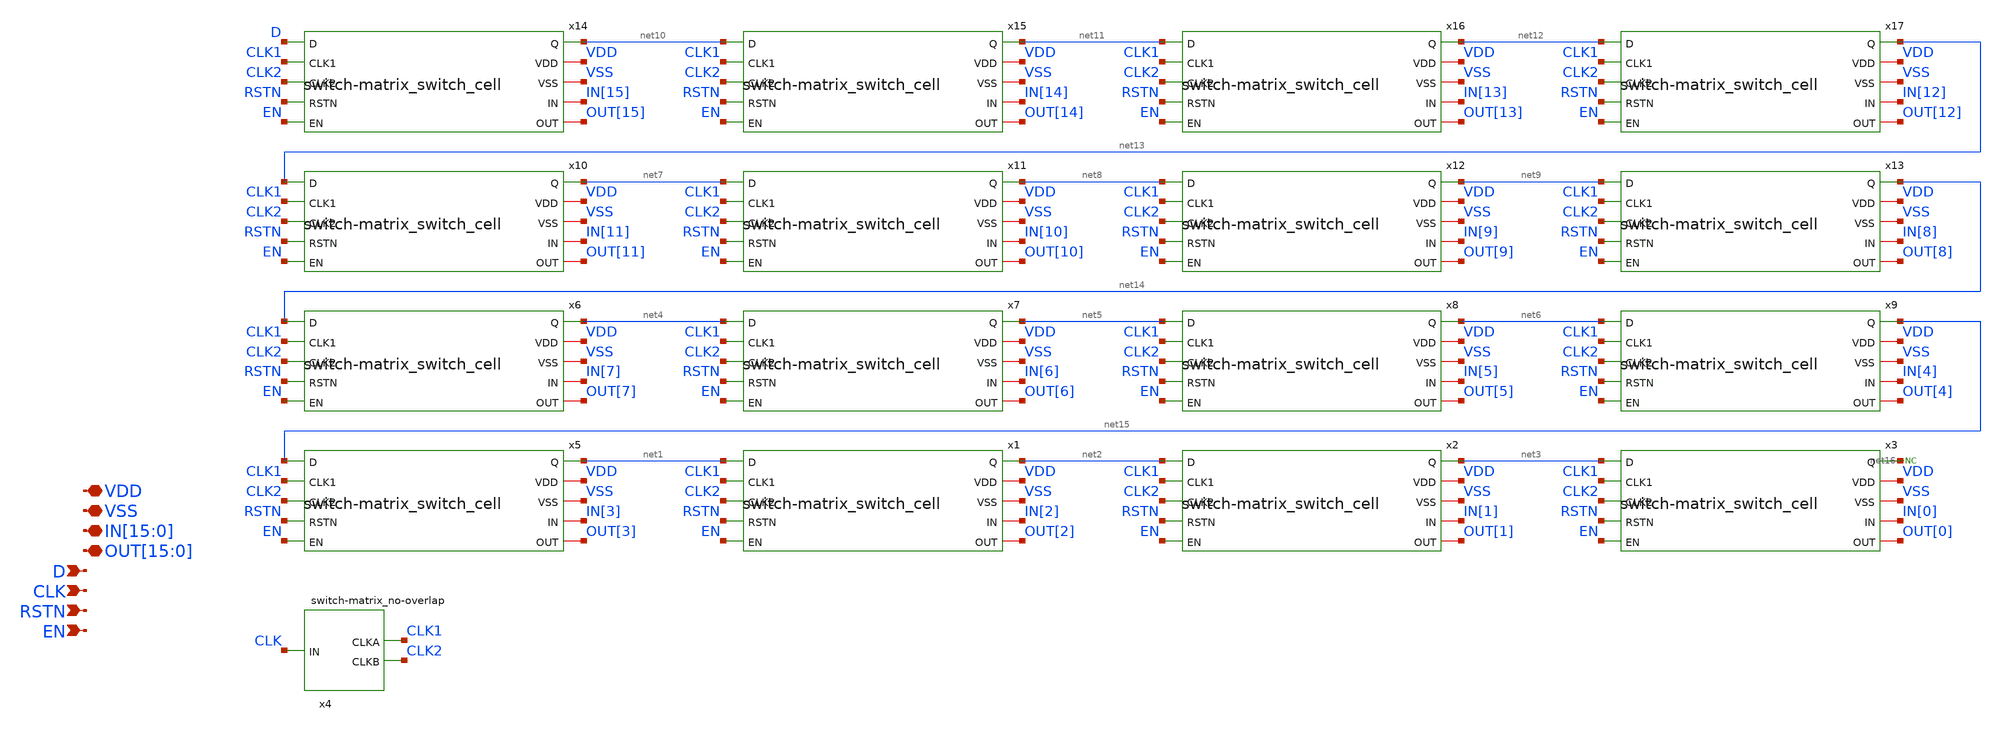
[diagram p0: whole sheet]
** sch_path: designs/libs/core_analog/switch-matrix/switch-matrix_tg_array_16x1.sch
**.subckt switch-matrix_tg_array_16x1 VDD VSS
*+ IN[15],IN[14],IN[13],IN[12],IN[11],IN[10],IN[9],IN[8],IN[7],IN[6],IN[5],IN[4],IN[3],IN[2],IN[1],IN[0]
*+ OUT[15],OUT[14],OUT[13],OUT[12],OUT[11],OUT[10],OUT[9],OUT[8],OUT[7],OUT[6],OUT[5],OUT[4],OUT[3],OUT[2],OUT[1],OUT[0] D RSTN CLK EN
*.iopin VDD
*.iopin VSS
*.iopin
*+ IN[15],IN[14],IN[13],IN[12],IN[11],IN[10],IN[9],IN[8],IN[7],IN[6],IN[5],IN[4],IN[3],IN[2],IN[1],IN[0]
*.iopin
*+ OUT[15],OUT[14],OUT[13],OUT[12],OUT[11],OUT[10],OUT[9],OUT[8],OUT[7],OUT[6],OUT[5],OUT[4],OUT[3],OUT[2],OUT[1],OUT[0]
*.ipin D
*.ipin RSTN
*.ipin CLK
*.ipin EN
* noconn #net16
x5 net1 VDD VSS net15 CLK1 CLK2 RSTN EN IN[3] OUT[3] switch-matrix_switch_cell
x1 net2 VDD VSS net1 CLK1 CLK2 RSTN EN IN[2] OUT[2] switch-matrix_switch_cell
x2 net3 VDD VSS net2 CLK1 CLK2 RSTN EN IN[1] OUT[1] switch-matrix_switch_cell
x3 net16 VDD VSS net3 CLK1 CLK2 RSTN EN IN[0] OUT[0] switch-matrix_switch_cell
x4 CLK VSS VDD CLK1 CLK2 switch-matrix_no-overlap
x6 net4 VDD VSS net14 CLK1 CLK2 RSTN EN IN[7] OUT[7] switch-matrix_switch_cell
x7 net5 VDD VSS net4 CLK1 CLK2 RSTN EN IN[6] OUT[6] switch-matrix_switch_cell
x8 net6 VDD VSS net5 CLK1 CLK2 RSTN EN IN[5] OUT[5] switch-matrix_switch_cell
x9 net15 VDD VSS net6 CLK1 CLK2 RSTN EN IN[4] OUT[4] switch-matrix_switch_cell
x10 net7 VDD VSS net13 CLK1 CLK2 RSTN EN IN[11] OUT[11] switch-matrix_switch_cell
x11 net8 VDD VSS net7 CLK1 CLK2 RSTN EN IN[10] OUT[10] switch-matrix_switch_cell
x12 net9 VDD VSS net8 CLK1 CLK2 RSTN EN IN[9] OUT[9] switch-matrix_switch_cell
x13 net14 VDD VSS net9 CLK1 CLK2 RSTN EN IN[8] OUT[8] switch-matrix_switch_cell
x14 net10 VDD VSS D CLK1 CLK2 RSTN EN IN[15] OUT[15] switch-matrix_switch_cell
x15 net11 VDD VSS net10 CLK1 CLK2 RSTN EN IN[14] OUT[14] switch-matrix_switch_cell
x16 net12 VDD VSS net11 CLK1 CLK2 RSTN EN IN[13] OUT[13] switch-matrix_switch_cell
x17 net13 VDD VSS net12 CLK1 CLK2 RSTN EN IN[12] OUT[12] switch-matrix_switch_cell
**.ends
.end
